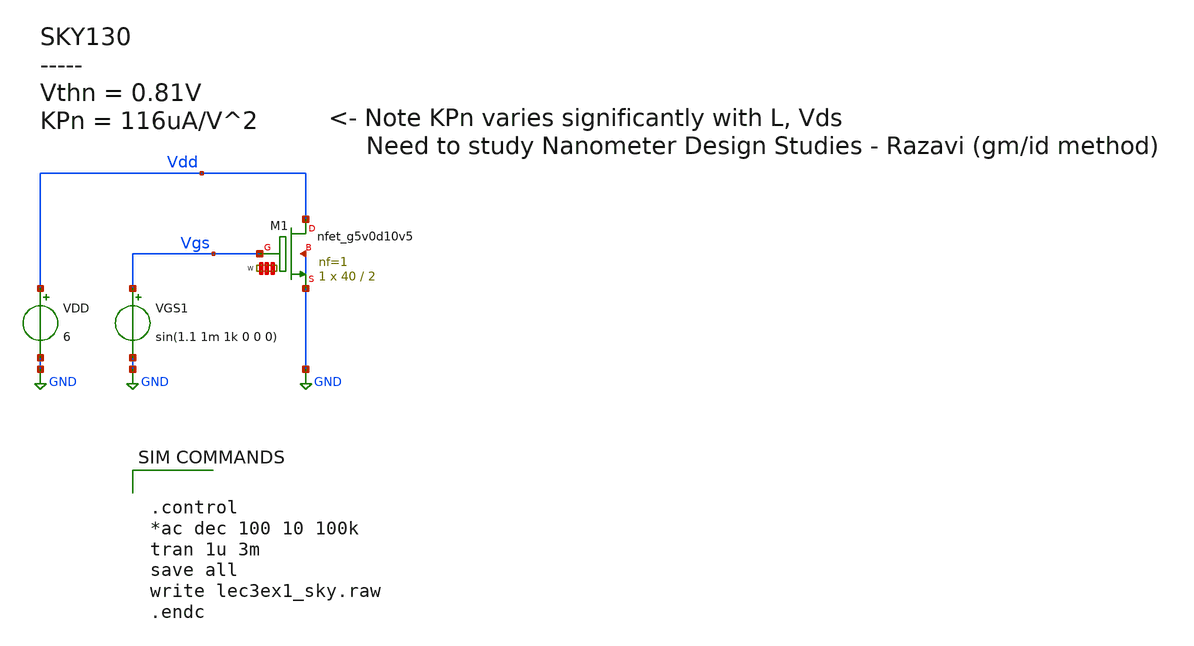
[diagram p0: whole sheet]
** sch_path: lec3ex1_sky.sch
**.subckt lec3ex1_sky
VGS1 Vgs GND sin(1.1 1m 1k 0 0 0)
VDD Vdd GND 6
XM1 Vdd Vgs GND GND sky130_fd_pr__nfet_g5v0d10v5 L=2 W='40 * 1 ' nf=1 ad='int((nf+1)/2) * W / nf * 0.29'
+ as='int((nf+2)/2) * W / nf * 0.29' pd='2*int((nf+1)/2) * (W / nf + 0.29)' ps='2*int((nf+2)/2) * (W / nf + 0.29)'
+ nrd='0.29 / W ' nrs='0.29 / W ' sa=0 sb=0 sd=0 mult=1 m=1
**** begin user architecture code


.control
*ac dec 100 10 100k
tran 1u 3m
save all
write lec3ex1_sky.raw
.endc



** opencircuitdesign pdks install
.lib $::SKYWATER_MODELS/sky130.lib.spice tt


**** end user architecture code
**.ends
.GLOBAL GND
.end
